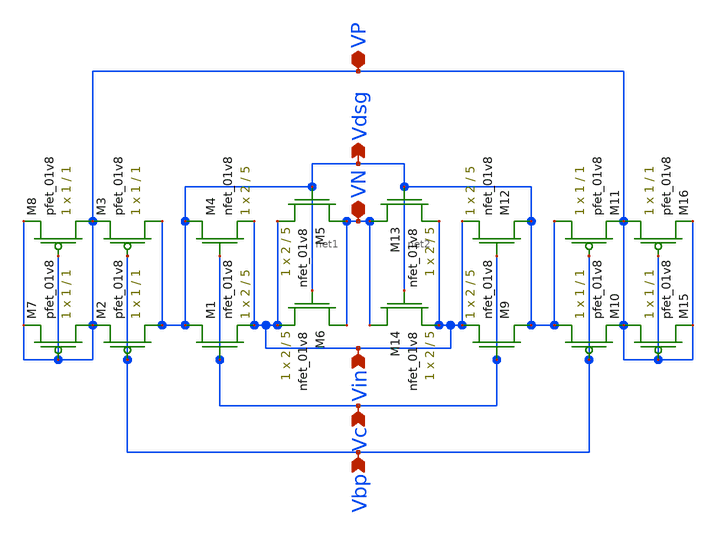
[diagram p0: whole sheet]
** sch_path: LDS/LDS_fvf.sch
**.subckt LDS_fvf VN Vin Vc Vdsg Vbp VP
*.iopin VN
*.ipin Vin
*.ipin Vc
*.opin Vdsg
*.ipin Vbp
*.iopin VP
XM1 Vdsg Vc Vin GND sky130_fd_pr__nfet_01v8 L=5 W=2 nf=1 ad='int((nf+1)/2) * W/nf * 0.29' as='int((nf+2)/2) * W/nf * 0.29'
+ pd='2*int((nf+1)/2) * (W/nf + 0.29)' ps='2*int((nf+2)/2) * (W/nf + 0.29)' nrd='0.29 / W' nrs='0.29 / W'
+ sa=0 sb=0 sd=0 mult=1 m=1
XM2 Vdsg Vbp VP VDD sky130_fd_pr__pfet_01v8 L=1 W=1 nf=1 ad='int((nf+1)/2) * W/nf * 0.29' as='int((nf+2)/2) * W/nf * 0.29'
+ pd='2*int((nf+1)/2) * (W/nf + 0.29)' ps='2*int((nf+2)/2) * (W/nf + 0.29)' nrd='0.29 / W' nrs='0.29 / W'
+ sa=0 sb=0 sd=0 mult=1 m=1
XM3 Vdsg Vbp VP VDD sky130_fd_pr__pfet_01v8 L=1 W=1 nf=1 ad='int((nf+1)/2) * W/nf * 0.29' as='int((nf+2)/2) * W/nf * 0.29'
+ pd='2*int((nf+1)/2) * (W/nf + 0.29)' ps='2*int((nf+2)/2) * (W/nf + 0.29)' nrd='0.29 / W' nrs='0.29 / W'
+ sa=0 sb=0 sd=0 mult=1 m=1
XM4 Vdsg Vc Vin GND sky130_fd_pr__nfet_01v8 L=5 W=2 nf=1 ad='int((nf+1)/2) * W/nf * 0.29' as='int((nf+2)/2) * W/nf * 0.29'
+ pd='2*int((nf+1)/2) * (W/nf + 0.29)' ps='2*int((nf+2)/2) * (W/nf + 0.29)' nrd='0.29 / W' nrs='0.29 / W'
+ sa=0 sb=0 sd=0 mult=1 m=1
XM5 VN Vdsg Vin GND sky130_fd_pr__nfet_01v8 L=5 W=2 nf=1 ad='int((nf+1)/2) * W/nf * 0.29' as='int((nf+2)/2) * W/nf * 0.29'
+ pd='2*int((nf+1)/2) * (W/nf + 0.29)' ps='2*int((nf+2)/2) * (W/nf + 0.29)' nrd='0.29 / W' nrs='0.29 / W'
+ sa=0 sb=0 sd=0 mult=1 m=1
XM6 VN net1 Vin GND sky130_fd_pr__nfet_01v8 L=5 W=2 nf=1 ad='int((nf+1)/2) * W/nf * 0.29' as='int((nf+2)/2) * W/nf * 0.29'
+ pd='2*int((nf+1)/2) * (W/nf + 0.29)' ps='2*int((nf+2)/2) * (W/nf + 0.29)' nrd='0.29 / W' nrs='0.29 / W'
+ sa=0 sb=0 sd=0 mult=1 m=1
XM7 VP VP VP VDD sky130_fd_pr__pfet_01v8 L=1 W=1 nf=1 ad='int((nf+1)/2) * W/nf * 0.29' as='int((nf+2)/2) * W/nf * 0.29'
+ pd='2*int((nf+1)/2) * (W/nf + 0.29)' ps='2*int((nf+2)/2) * (W/nf + 0.29)' nrd='0.29 / W' nrs='0.29 / W'
+ sa=0 sb=0 sd=0 mult=1 m=1
XM8 VP VP VP VDD sky130_fd_pr__pfet_01v8 L=1 W=1 nf=1 ad='int((nf+1)/2) * W/nf * 0.29' as='int((nf+2)/2) * W/nf * 0.29'
+ pd='2*int((nf+1)/2) * (W/nf + 0.29)' ps='2*int((nf+2)/2) * (W/nf + 0.29)' nrd='0.29 / W' nrs='0.29 / W'
+ sa=0 sb=0 sd=0 mult=1 m=1
XM9 Vdsg Vc Vin GND sky130_fd_pr__nfet_01v8 L=5 W=2 nf=1 ad='int((nf+1)/2) * W/nf * 0.29' as='int((nf+2)/2) * W/nf * 0.29'
+ pd='2*int((nf+1)/2) * (W/nf + 0.29)' ps='2*int((nf+2)/2) * (W/nf + 0.29)' nrd='0.29 / W' nrs='0.29 / W'
+ sa=0 sb=0 sd=0 mult=1 m=1
XM10 Vdsg Vbp VP VDD sky130_fd_pr__pfet_01v8 L=1 W=1 nf=1 ad='int((nf+1)/2) * W/nf * 0.29' as='int((nf+2)/2) * W/nf * 0.29'
+ pd='2*int((nf+1)/2) * (W/nf + 0.29)' ps='2*int((nf+2)/2) * (W/nf + 0.29)' nrd='0.29 / W' nrs='0.29 / W'
+ sa=0 sb=0 sd=0 mult=1 m=1
XM11 Vdsg Vbp VP VDD sky130_fd_pr__pfet_01v8 L=1 W=1 nf=1 ad='int((nf+1)/2) * W/nf * 0.29' as='int((nf+2)/2) * W/nf * 0.29'
+ pd='2*int((nf+1)/2) * (W/nf + 0.29)' ps='2*int((nf+2)/2) * (W/nf + 0.29)' nrd='0.29 / W' nrs='0.29 / W'
+ sa=0 sb=0 sd=0 mult=1 m=1
XM12 Vdsg Vc Vin GND sky130_fd_pr__nfet_01v8 L=5 W=2 nf=1 ad='int((nf+1)/2) * W/nf * 0.29' as='int((nf+2)/2) * W/nf * 0.29'
+ pd='2*int((nf+1)/2) * (W/nf + 0.29)' ps='2*int((nf+2)/2) * (W/nf + 0.29)' nrd='0.29 / W' nrs='0.29 / W'
+ sa=0 sb=0 sd=0 mult=1 m=1
XM13 VN Vdsg Vin GND sky130_fd_pr__nfet_01v8 L=5 W=2 nf=1 ad='int((nf+1)/2) * W/nf * 0.29' as='int((nf+2)/2) * W/nf * 0.29'
+ pd='2*int((nf+1)/2) * (W/nf + 0.29)' ps='2*int((nf+2)/2) * (W/nf + 0.29)' nrd='0.29 / W' nrs='0.29 / W'
+ sa=0 sb=0 sd=0 mult=1 m=1
XM14 VN net2 Vin GND sky130_fd_pr__nfet_01v8 L=5 W=2 nf=1 ad='int((nf+1)/2) * W/nf * 0.29' as='int((nf+2)/2) * W/nf * 0.29'
+ pd='2*int((nf+1)/2) * (W/nf + 0.29)' ps='2*int((nf+2)/2) * (W/nf + 0.29)' nrd='0.29 / W' nrs='0.29 / W'
+ sa=0 sb=0 sd=0 mult=1 m=1
XM15 VP VP VP VDD sky130_fd_pr__pfet_01v8 L=1 W=1 nf=1 ad='int((nf+1)/2) * W/nf * 0.29' as='int((nf+2)/2) * W/nf * 0.29'
+ pd='2*int((nf+1)/2) * (W/nf + 0.29)' ps='2*int((nf+2)/2) * (W/nf + 0.29)' nrd='0.29 / W' nrs='0.29 / W'
+ sa=0 sb=0 sd=0 mult=1 m=1
XM16 VP VP VP VDD sky130_fd_pr__pfet_01v8 L=1 W=1 nf=1 ad='int((nf+1)/2) * W/nf * 0.29' as='int((nf+2)/2) * W/nf * 0.29'
+ pd='2*int((nf+1)/2) * (W/nf + 0.29)' ps='2*int((nf+2)/2) * (W/nf + 0.29)' nrd='0.29 / W' nrs='0.29 / W'
+ sa=0 sb=0 sd=0 mult=1 m=1
**.ends
.end
